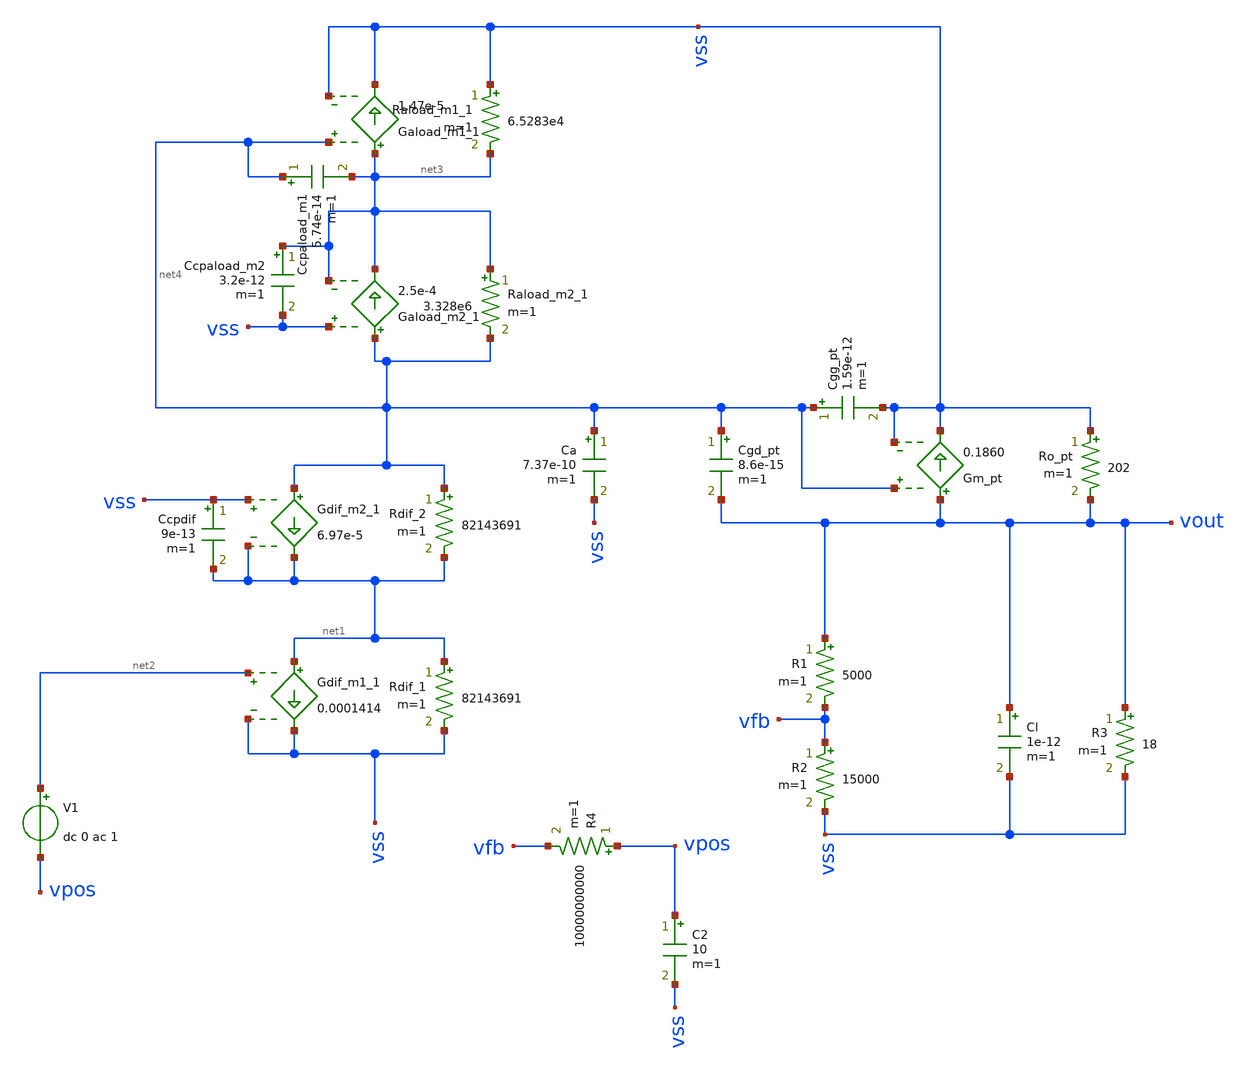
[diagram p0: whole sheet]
** sch_path: test/Tesis_notebooks/xschem/ldo_ol_cap.sch
**.subckt ldo_ol_cap
Gdif_m1_1 net1 vss net2 vss 0.0001414
Raload_m1_1 vss net3 6.5283e4 m=1
Gaload_m1_1 net3 vss net4 vss 1.47e-5
Gdif_m2_1 net4 net1 vss net1 6.97e-5
Ccpdif vss net1 9e-13 m=1
Raload_m2_1 net3 net4 3.328e6 m=1
Gaload_m2_1 net4 net3 vss net3 2.5e-4
Ccpaload_m1 net4 net3 5.74e-14 m=1
Ccpaload_m2 net3 vss 3.2e-12 m=1
R1 vout vfb 5000 m=1
R2 vfb vss 15000 m=1
Ro_pt vss vout 202 m=1
Gm_pt vout vss net4 vss 0.1860
Cgg_pt net4 vss 1.59e-12 m=1
Cgd_pt net4 vout 8.6e-15 m=1
R4 vpos vfb 10000000000 m=1
C2 vpos vss 10 m=1
V1 net2 vpos dc 0 ac 1
Cl vout vss 1e-12 m=1
R3 vout vss 18 m=1
Ca net4 vss 7.37e-10 m=1
Rdif_1 net1 vss 82143691 m=1
Rdif_2 net4 net1 82143691 m=1
**** begin user architecture code



.lib /opt/pdks/sky130A/libs.tech/ngspice/sky130.lib.spice tt

Vss vss 0 0

.control
ac dec 10 1 10G
plot vdb(vout)
plot phase(vout)*180/PI
.endc



**** end user architecture code
**.ends
.end
